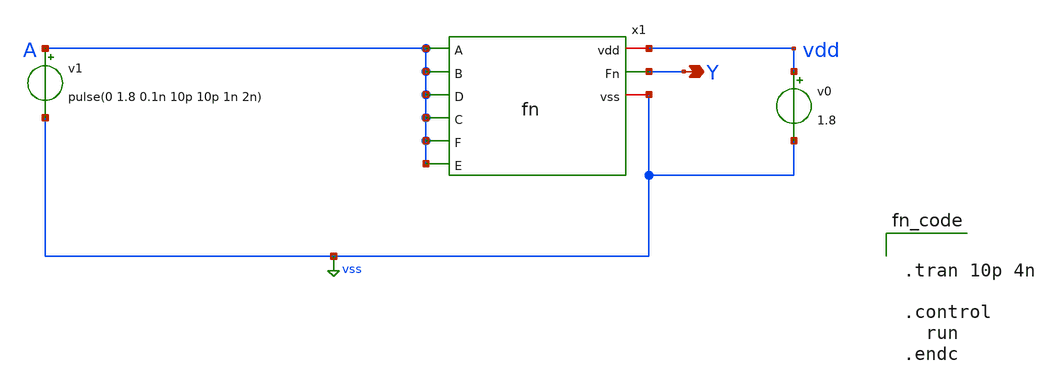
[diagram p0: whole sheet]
** sch_path: week0/netlists/xschem/fn/schematic/fn_spice.sch
**.subckt fn_spice Y
*.opin Y
x1 vdd A A A A A A Y vss fn
v0 vdd vss 1.8
v1 A vss pulse(0 1.8 0.1n 10p 10p 1n 2n)
**** begin user architecture code


.lib /usr/local/share/pdk/sky130A/libs.tech/ngspice/sky130.lib.spice tt




.tran 10p 4n

.control
  run
.endc


**** end user architecture code
**.ends
.GLOBAL vss
.end
